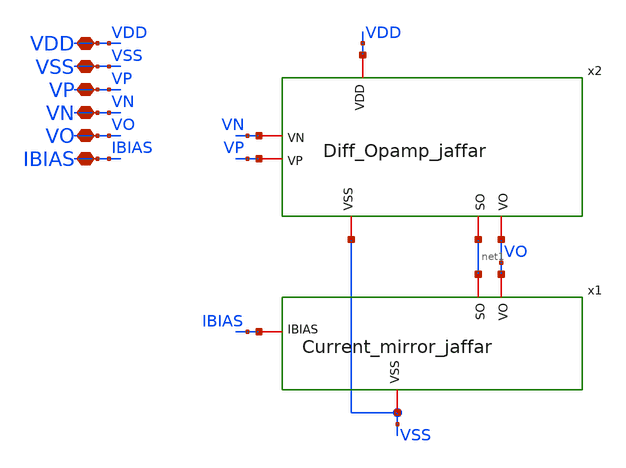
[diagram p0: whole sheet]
** sch_path: xschem/xschem_BGR_Top/Opamp_Jaffar_withBlocks.sch
**.subckt Opamp_Jaffar_withBlocks VDD VSS VP VN VO IBIAS
*.iopin VDD
*.iopin VSS
*.iopin VP
*.iopin VN
*.iopin VO
*.iopin IBIAS
x1 VSS VO IBIAS net1 Current_mirror_jaffar
x2 VDD VSS VP VN net1 VO Diff_Opamp_jaffar
**.ends
.end
